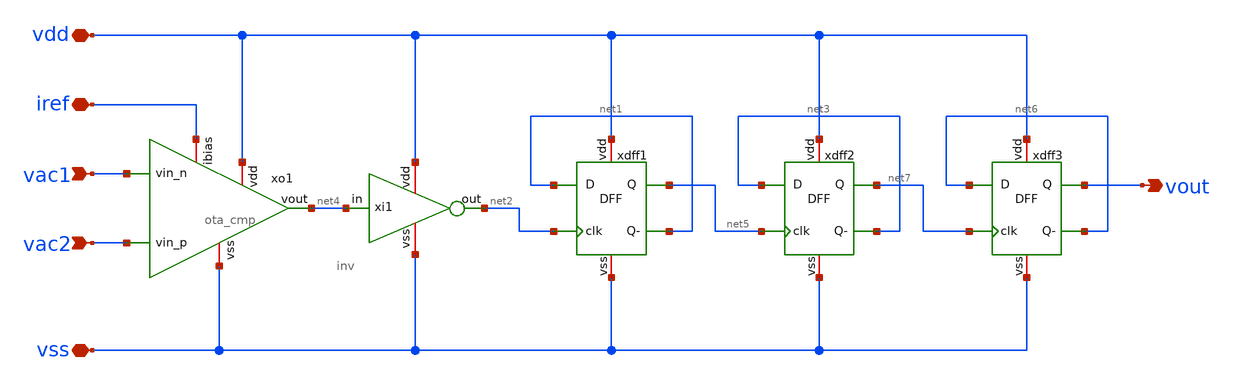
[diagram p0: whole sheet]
** sch_path: SSDOR_1.2V_v2/components/cgenerator/cgenerator.sch
**.subckt cgenerator vdd vss iref vac1 vac2 vout
*.iopin vdd
*.iopin vss
*.iopin iref
*.ipin vac1
*.ipin vac2
*.opin vout
xi1 vdd net4 net2 vss inv
xo1 vdd iref net4 vac1 vac2 vss ota_cmp
xdff1 net1 net5 net1 vdd vss net2 dff
xdff2 net3 net7 net3 vdd vss net5 dff
xdff3 net6 vout net6 vdd vss net7 dff
**.ends

* expanding   symbol:
*+  /home/designer/shared/designs/SSDOR_1.2V_v2_test/components/cgenerator/inv.sym # of pins=4
** sym_path: SSDOR_1.2V_v2/components/cgenerator/inv.sym
** sch_path: SSDOR_1.2V_v2/components/cgenerator/inv.sch
.subckt inv vdd in out vss
*.iopin vdd
*.iopin vss
*.ipin in
*.opin out
XM1 out in vss vss sg13_lv_nmos w=1u l=0.13u ng=1 m=1 mm_ok=1
XM2 out in vdd vdd sg13_lv_pmos w=1.9u l=0.13u ng=1 m=1 mm_ok=1
.ends


* expanding   symbol:
*+  /home/designer/shared/designs/SSDOR_1.2V_v2_test/components/cgenerator/ota_cmp.sym # of pins=6
** sym_path: SSDOR_1.2V_v2/components/cgenerator/ota_cmp.sym
** sch_path: SSDOR_1.2V_v2/components/cgenerator/ota_cmp.sch
.subckt ota_cmp vdd ibias vout vin_n vin_p vss
*.iopin vdd
*.iopin vss
*.iopin ibias
*.ipin vin_p
*.ipin vin_n
*.opin vout
XM1 vbn1 vin_p vp vp sg13_lv_pmos w=10u l=0.5u ng=1 m=1 mm_ok=1
XM2 vbn2 vin_n vp vp sg13_lv_pmos w=10u l=0.5u ng=1 m=1 mm_ok=1
XM5 vp vbp1 vdd vdd sg13_lv_pmos w=10u l=0.5u ng=1 m=1 mm_ok=1
XM3 vbn1 vbn1 vss vss sg13_lv_nmos w=1u l=0.5u ng=1 m=1 mm_ok=1
XM4 vbn2 vbn2 vss vss sg13_lv_nmos w=1u l=0.5u ng=1 m=1 mm_ok=1
XM6 vout vbn2 vss vss sg13_lv_nmos w=1u l=0.5u ng=1 m=1 mm_ok=1
XM7 vbp2 vbn1 vss vss sg13_lv_nmos w=1u l=0.5u ng=1 m=1 mm_ok=1
XM8 vout vbp2 vdd vdd sg13_lv_pmos w=1u l=0.5u ng=1 m=1 mm_ok=1
XM9 vbp2 vbp2 vdd vdd sg13_lv_pmos w=1u l=0.5u ng=1 m=1 mm_ok=1
XM10 vbp1 vbp1 vdd vdd sg13_lv_pmos w=10u l=0.5u ng=1 m=1 mm_ok=1
XM11 vbp1 ibias vss vss sg13_lv_nmos w=1u l=0.5u ng=1 m=1 mm_ok=1
XM12 ibias ibias vss vss sg13_lv_nmos w=1u l=0.5u ng=1 m=1 mm_ok=1
.ends


* expanding   symbol:
*+  /home/designer/shared/designs/SSDOR_1.2V_v2_test/components/cgenerator/dff.sym # of pins=6
** sym_path: SSDOR_1.2V_v2/components/cgenerator/dff.sym
** sch_path: SSDOR_1.2V_v2/components/cgenerator/dff.sch
.subckt dff D Q Q- vdd vss clk
*.ipin clk
*.iopin vdd
*.opin Q
*.iopin vss
*.ipin D
*.opin Q-
XM1 clk- clk vss vss sg13_lv_nmos w=1u l=0.13u ng=1 m=1 mm_ok=1
XM2 clk- clk vdd vdd sg13_lv_pmos w=1.9u l=0.13u ng=1 m=1 mm_ok=1
XM3 net2 net1 vss vss sg13_lv_nmos w=1u l=0.13u ng=1 m=1 mm_ok=1
XM4 net2 net1 vdd vdd sg13_lv_pmos w=1.9u l=0.13u ng=1 m=1 mm_ok=1
XM5 net1 clk D vdd sg13_lv_pmos w=10u l=0.13u ng=1 m=2 mm_ok=1
XM6 net1 clk- D vss sg13_lv_nmos w=10u l=0.13u ng=1 m=1 mm_ok=1
XM9 net3 net2 vss vss sg13_lv_nmos w=0.5u l=0.13u ng=1 m=1 mm_ok=1
XM10 net3 net2 vdd vdd sg13_lv_pmos w=1u l=0.13u ng=1 m=1 mm_ok=1
XM7 net3 clk net1 vdd sg13_lv_pmos w=10u l=0.13u ng=1 m=2 mm_ok=1
XM8 net3 clk- net1 vss sg13_lv_nmos w=10u l=0.13u ng=1 m=1 mm_ok=1
XM11 net4 clk- net2 vdd sg13_lv_pmos w=10u l=0.13u ng=1 m=2 mm_ok=1
XM12 net4 clk net2 vss sg13_lv_nmos w=10u l=0.13u ng=1 m=1 mm_ok=1
XM13 Q net4 vss vss sg13_lv_nmos w=1u l=0.13u ng=1 m=1 mm_ok=1
XM14 Q net4 vdd vdd sg13_lv_pmos w=1.9u l=0.13u ng=1 m=1 mm_ok=1
XM15 net5 Q vss vss sg13_lv_nmos w=0.5u l=0.13u ng=1 m=1 mm_ok=1
XM16 net5 Q vdd vdd sg13_lv_pmos w=1u l=0.13u ng=1 m=1 mm_ok=1
XM17 net5 clk- net4 vdd sg13_lv_pmos w=10u l=0.13u ng=1 m=2 mm_ok=1
XM18 net5 clk net4 vss sg13_lv_nmos w=10u l=0.13u ng=1 m=1 mm_ok=1
XM19 Q- Q vss vss sg13_lv_nmos w=1u l=0.13u ng=1 m=1 mm_ok=1
XM20 Q- Q vdd vdd sg13_lv_pmos w=1.9u l=0.13u ng=1 m=1 mm_ok=1
.ends

.end
